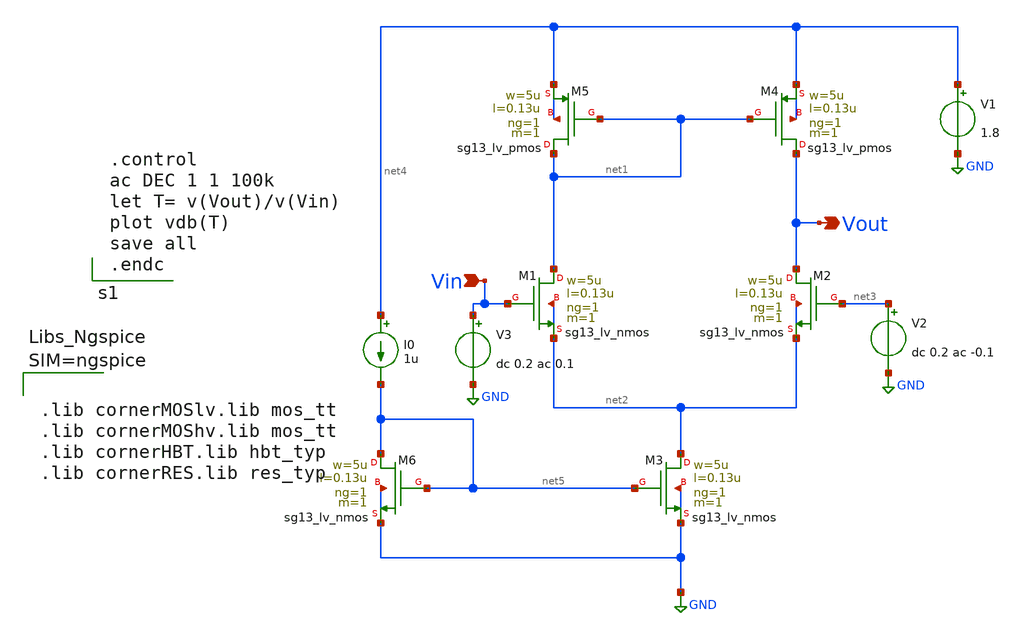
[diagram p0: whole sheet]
** sch_path: 5T.sch
**.subckt 5T Vout Vin
*.opin Vout
*.ipin Vin
XM1 net1 Vin net2 net2 sg13_lv_nmos w=5u l=0.13u ng=1 m=1 mm_ok=1
XM2 Vout net3 net2 net2 sg13_lv_nmos w=5u l=0.13u ng=1 m=1 mm_ok=1
XM3 net2 net5 GND GND sg13_lv_nmos w=5u l=0.13u ng=1 m=1 mm_ok=1
XM4 Vout net1 net4 net4 sg13_lv_pmos w=5u l=0.13u ng=1 m=1 mm_ok=1
XM5 net1 net1 net4 net4 sg13_lv_pmos w=5u l=0.13u ng=1 m=1 mm_ok=1
V1 net4 GND 1.8
V2 net3 GND dc 0.2 ac -0.1
V3 Vin GND dc 0.2 ac 0.1
XM6 net5 net5 GND GND sg13_lv_nmos w=5u l=0.13u ng=1 m=1 mm_ok=1
I0 net4 net5 1u
**** begin user architecture code


.control
ac DEC 1 1 100k
let T= v(Vout)/v(Vin)
plot vdb(T)
save all
.endc





.lib cornerMOSlv.lib mos_tt
.lib cornerMOShv.lib mos_tt
.lib cornerHBT.lib hbt_typ
.lib cornerRES.lib res_typ



**** end user architecture code
**.ends
.GLOBAL GND
.end
